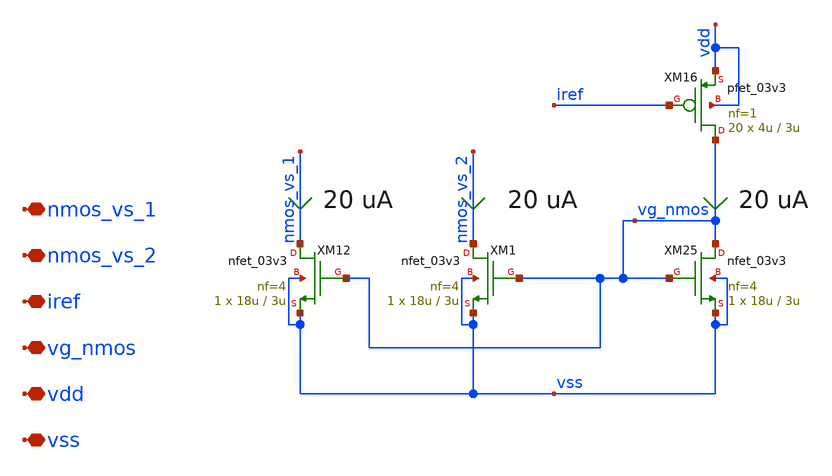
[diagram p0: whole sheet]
** sch_path: xschem/ccia_rrl_ota/b9_ccia_rrl_ota_nmos_bias.sch
**.subckt b9_ccia_rrl_ota_nmos_bias nmos_vs_1 nmos_vs_2 iref vdd vss vg_nmos
*.iopin nmos_vs_1
*.iopin nmos_vs_2
*.iopin iref
*.iopin vdd
*.iopin vss
*.iopin vg_nmos
XM16 vg_nmos iref vdd vdd pfet_03v3 L=3u W=4u nf=1 ad='int((nf+1)/2) * W/nf * 0.18u' as='int((nf+2)/2) * W/nf * 0.18u'
+ pd='2*int((nf+1)/2) * (W/nf + 0.18u)' ps='2*int((nf+2)/2) * (W/nf + 0.18u)' nrd='0.18u / W' nrs='0.18u / W'
+ sa=0 sb=0 sd=0 m=20
XM12 nmos_vs_1 vg_nmos vss vss nfet_03v3 L=3u W=18u nf=4 ad='int((nf+1)/2) * W/nf * 0.18u' as='int((nf+2)/2) * W/nf * 0.18u'
+ pd='2*int((nf+1)/2) * (W/nf + 0.18u)' ps='2*int((nf+2)/2) * (W/nf + 0.18u)' nrd='0.18u / W' nrs='0.18u / W'
+ sa=0 sb=0 sd=0 m=1
XM25 vg_nmos vg_nmos vss vss nfet_03v3 L=3u W=18u nf=4 ad='int((nf+1)/2) * W/nf * 0.18u' as='int((nf+2)/2) * W/nf * 0.18u'
+ pd='2*int((nf+1)/2) * (W/nf + 0.18u)' ps='2*int((nf+2)/2) * (W/nf + 0.18u)' nrd='0.18u / W' nrs='0.18u / W'
+ sa=0 sb=0 sd=0 m=1
XM1 nmos_vs_2 vg_nmos vss vss nfet_03v3 L=3u W=18u nf=4 ad='int((nf+1)/2) * W/nf * 0.18u' as='int((nf+2)/2) * W/nf * 0.18u'
+ pd='2*int((nf+1)/2) * (W/nf + 0.18u)' ps='2*int((nf+2)/2) * (W/nf + 0.18u)' nrd='0.18u / W' nrs='0.18u / W'
+ sa=0 sb=0 sd=0 m=1
**.ends
.end
